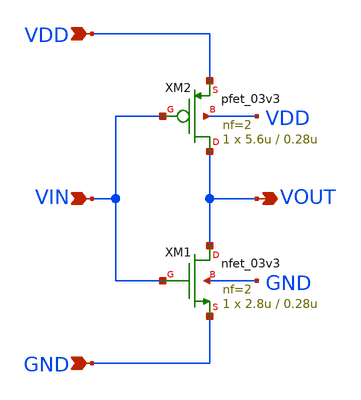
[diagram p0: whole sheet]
** sch_path: Design_Files/Inverter/SA_INV_1X.sch
**.subckt SA_INV_1X VIN VDD GND VOUT
*.ipin VIN
*.ipin VDD
*.ipin GND
*.opin VOUT
XM1 VOUT VIN GND GND nfet_03v3 L=0.28u W=2.8u nf=2 ad='int((nf+1)/2) * W/nf * 0.18u' as='int((nf+2)/2) * W/nf * 0.18u'
+ pd='2*int((nf+1)/2) * (W/nf + 0.18u)' ps='2*int((nf+2)/2) * (W/nf + 0.18u)' nrd='0.18u / W' nrs='0.18u / W'
+ sa=0 sb=0 sd=0 m=1
XM2 VOUT VIN VDD VDD pfet_03v3 L=0.28u W=5.6u nf=2 ad='int((nf+1)/2) * W/nf * 0.18u' as='int((nf+2)/2) * W/nf * 0.18u'
+ pd='2*int((nf+1)/2) * (W/nf + 0.18u)' ps='2*int((nf+2)/2) * (W/nf + 0.18u)' nrd='0.18u / W' nrs='0.18u / W'
+ sa=0 sb=0 sd=0 m=1
**.ends
.end
